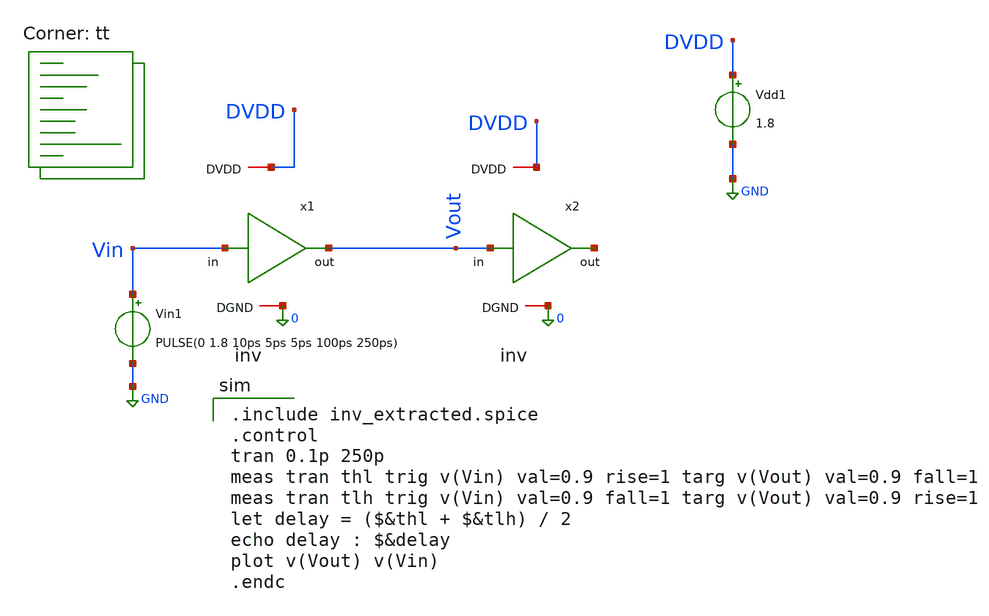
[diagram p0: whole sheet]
** sch_path: tutorial-4/source/q1a/q1a.sch
**.subckt q1a
Vin1 Vin GND PULSE(0 1.8 10ps 5ps 5ps 100ps 250ps)
Vdd1 DVDD GND 1.8
x1 Vin Vout DVDD 0 inv
x2 Vout net1 DVDD 0 inv
**** begin user architecture code
.lib $::SKYWATER_MODELS/sky130.lib.spice tt

.include inv_extracted.spice
.control
tran 0.1p 250p
meas tran thl trig v(Vin) val=0.9 rise=1 targ v(Vout) val=0.9 fall=1
meas tran tlh trig v(Vin) val=0.9 fall=1 targ v(Vout) val=0.9 rise=1
let delay = ($&thl + $&tlh) / 2
echo delay : $&delay
plot v(Vout) v(Vin)
.endc

**** end user architecture code
**.ends
.GLOBAL GND
.end
